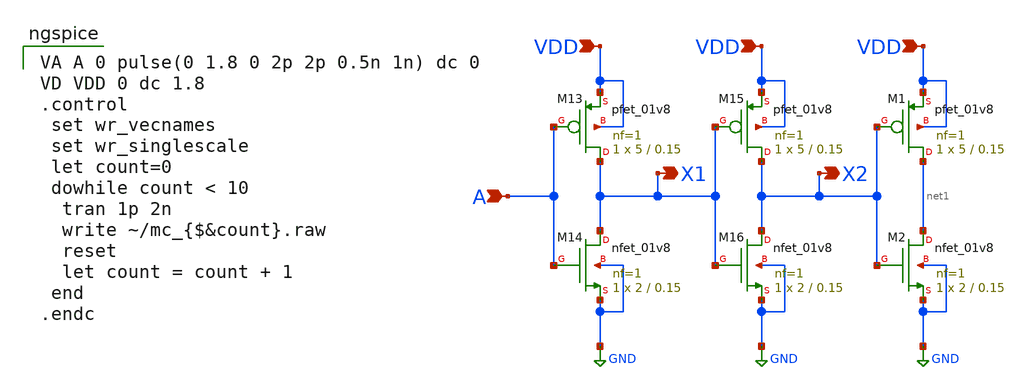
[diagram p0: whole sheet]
** sch_path: test_inv_mc.sch
**.subckt test_inv_mc VDD A VDD VDD X1 X2
*.ipin VDD
*.ipin A
*.ipin VDD
*.ipin VDD
*.opin X1
*.opin X2
XM13 X1 A VDD VDD sky130_fd_pr__pfet_01v8 L=0.15 W=5 nf=1 ad='int((nf+1)/2) * W/nf * 0.29' as='int((nf+2)/2) * W/nf * 0.29'
+ pd='2*int((nf+1)/2) * (W/nf + 0.29)' ps='2*int((nf+2)/2) * (W/nf + 0.29)' nrd='0.29 / W' nrs='0.29 / W'
+ sa=0 sb=0 sd=0 mult=1 m=1
XM14 X1 A GND GND sky130_fd_pr__nfet_01v8 L=0.15 W=2 nf=1 ad='int((nf+1)/2) * W/nf * 0.29' as='int((nf+2)/2) * W/nf * 0.29'
+ pd='2*int((nf+1)/2) * (W/nf + 0.29)' ps='2*int((nf+2)/2) * (W/nf + 0.29)' nrd='0.29 / W' nrs='0.29 / W'
+ sa=0 sb=0 sd=0 mult=1 m=1
XM15 X2 X1 VDD VDD sky130_fd_pr__pfet_01v8 L=0.15 W=5 nf=1 ad='int((nf+1)/2) * W/nf * 0.29' as='int((nf+2)/2) * W/nf * 0.29'
+ pd='2*int((nf+1)/2) * (W/nf + 0.29)' ps='2*int((nf+2)/2) * (W/nf + 0.29)' nrd='0.29 / W' nrs='0.29 / W'
+ sa=0 sb=0 sd=0 mult=1 m=1
XM16 X2 X1 GND GND sky130_fd_pr__nfet_01v8 L=0.15 W=2 nf=1 ad='int((nf+1)/2) * W/nf * 0.29' as='int((nf+2)/2) * W/nf * 0.29'
+ pd='2*int((nf+1)/2) * (W/nf + 0.29)' ps='2*int((nf+2)/2) * (W/nf + 0.29)' nrd='0.29 / W' nrs='0.29 / W'
+ sa=0 sb=0 sd=0 mult=1 m=1
XM1 net1 X2 VDD VDD sky130_fd_pr__pfet_01v8 L=0.15 W=5 nf=1 ad='int((nf+1)/2) * W/nf * 0.29' as='int((nf+2)/2) * W/nf * 0.29'
+ pd='2*int((nf+1)/2) * (W/nf + 0.29)' ps='2*int((nf+2)/2) * (W/nf + 0.29)' nrd='0.29 / W' nrs='0.29 / W'
+ sa=0 sb=0 sd=0 mult=1 m=1
XM2 net1 X2 GND GND sky130_fd_pr__nfet_01v8 L=0.15 W=2 nf=1 ad='int((nf+1)/2) * W/nf * 0.29' as='int((nf+2)/2) * W/nf * 0.29'
+ pd='2*int((nf+1)/2) * (W/nf + 0.29)' ps='2*int((nf+2)/2) * (W/nf + 0.29)' nrd='0.29 / W' nrs='0.29 / W'
+ sa=0 sb=0 sd=0 mult=1 m=1
**** begin user architecture code

VA A 0 pulse(0 1.8 0 2p 2p 0.5n 1n) dc 0
VD VDD 0 dc 1.8
.control
 set wr_vecnames
 set wr_singlescale
 let count=0
 dowhile count < 10
  tran 1p 2n
  write ~/mc_{$&count}.raw
  reset
  let count = count + 1
 end
.endc


** opencircuitdesign pdks install
.lib $::SKYWATER_MODELS/sky130.lib.spice tt_mm

**** end user architecture code
**.ends
.GLOBAL GND
.end
